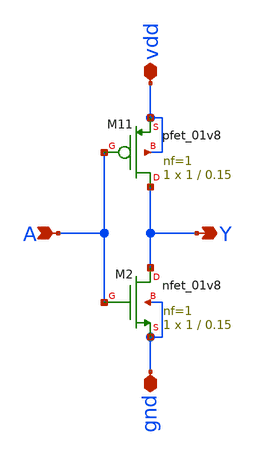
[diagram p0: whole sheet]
** sch_path: top/test/design/inv/inv.sch
**.subckt inv A Y vdd gnd
*.ipin A
*.opin Y
*.iopin vdd
*.iopin gnd
XM11 Y A vdd vdd sky130_fd_pr__pfet_01v8 L=0.15 W=1 nf=1 ad='int((nf+1)/2) * W/nf * 0.29' as='int((nf+2)/2) * W/nf * 0.29'
+ pd='2*int((nf+1)/2) * (W/nf + 0.29)' ps='2*int((nf+2)/2) * (W/nf + 0.29)' nrd='0.29 / W' nrs='0.29 / W'
+ sa=0 sb=0 sd=0 mult=1 m=1
XM2 Y A gnd gnd sky130_fd_pr__nfet_01v8 L=0.15 W=1 nf=1 ad='int((1 + 1)/2) * 1 / 1 * 0.29' as='int((1 + 2)/2) * 1 / 1 * 0.29'
+ pd='2*int((1 + 1)/2) * (1 / 1 + 0.29)' ps='2*int((1 + 2)/2) * (1 / 1 + 0.29)' nrd='0.29 / 1 ' nrs='0.29 / 1 '
+ sa=0 sb=0 sd=0 mult=1 m=1
**.ends
.end
